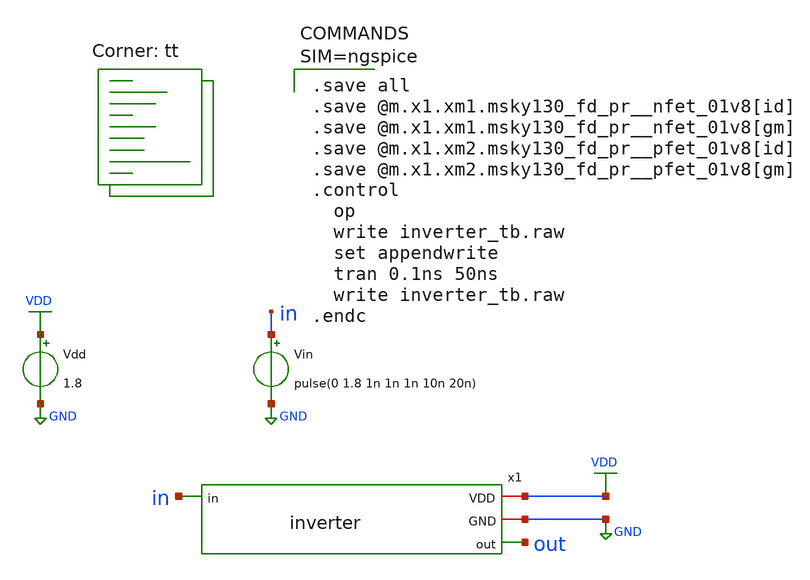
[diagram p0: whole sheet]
** sch_path: inverter_tb.sch
**.subckt inverter_tb
x1 VDD GND out in inverter
Vdd VDD GND 1.8
Vin in GND pulse(0 1.8 1n 1n 1n 10n 20n)
**** begin user architecture code
.lib $::SKYWATER_MODELS/sky130.lib.spice tt


.save all
.save @m.x1.xm1.msky130_fd_pr__nfet_01v8[id]
.save @m.x1.xm1.msky130_fd_pr__nfet_01v8[gm]
.save @m.x1.xm2.msky130_fd_pr__pfet_01v8[id]
.save @m.x1.xm2.msky130_fd_pr__pfet_01v8[gm]
.control
  op
  write inverter_tb.raw
  set appendwrite
  tran 0.1ns 50ns
  write inverter_tb.raw
.endc


**** end user architecture code
**.ends

* expanding   symbol:  inverter.sym # of pins=4
** sym_path: inverter.sym
** sch_path: inverter.sch
.subckt inverter VDD GND out in
*.opin out
*.ipin in
*.iopin VDD
*.iopin GND
XM1 out in GND GND sky130_fd_pr__nfet_01v8 L=0.15 W=1 nf=1 ad='int((nf+1)/2) * W/nf * 0.29' as='int((nf+2)/2) * W/nf * 0.29'
+ pd='2*int((nf+1)/2) * (W/nf + 0.29)' ps='2*int((nf+2)/2) * (W/nf + 0.29)' nrd='0.29 / W' nrs='0.29 / W'
+ sa=0 sb=0 sd=0 mult=1 m=1
XM2 out in VDD VDD sky130_fd_pr__pfet_01v8 L=0.15 W=1 nf=1 ad='int((nf+1)/2) * W/nf * 0.29' as='int((nf+2)/2) * W/nf * 0.29'
+ pd='2*int((nf+1)/2) * (W/nf + 0.29)' ps='2*int((nf+2)/2) * (W/nf + 0.29)' nrd='0.29 / W' nrs='0.29 / W'
+ sa=0 sb=0 sd=0 mult=1 m=1
.ends

.GLOBAL GND
.GLOBAL VDD
.end
